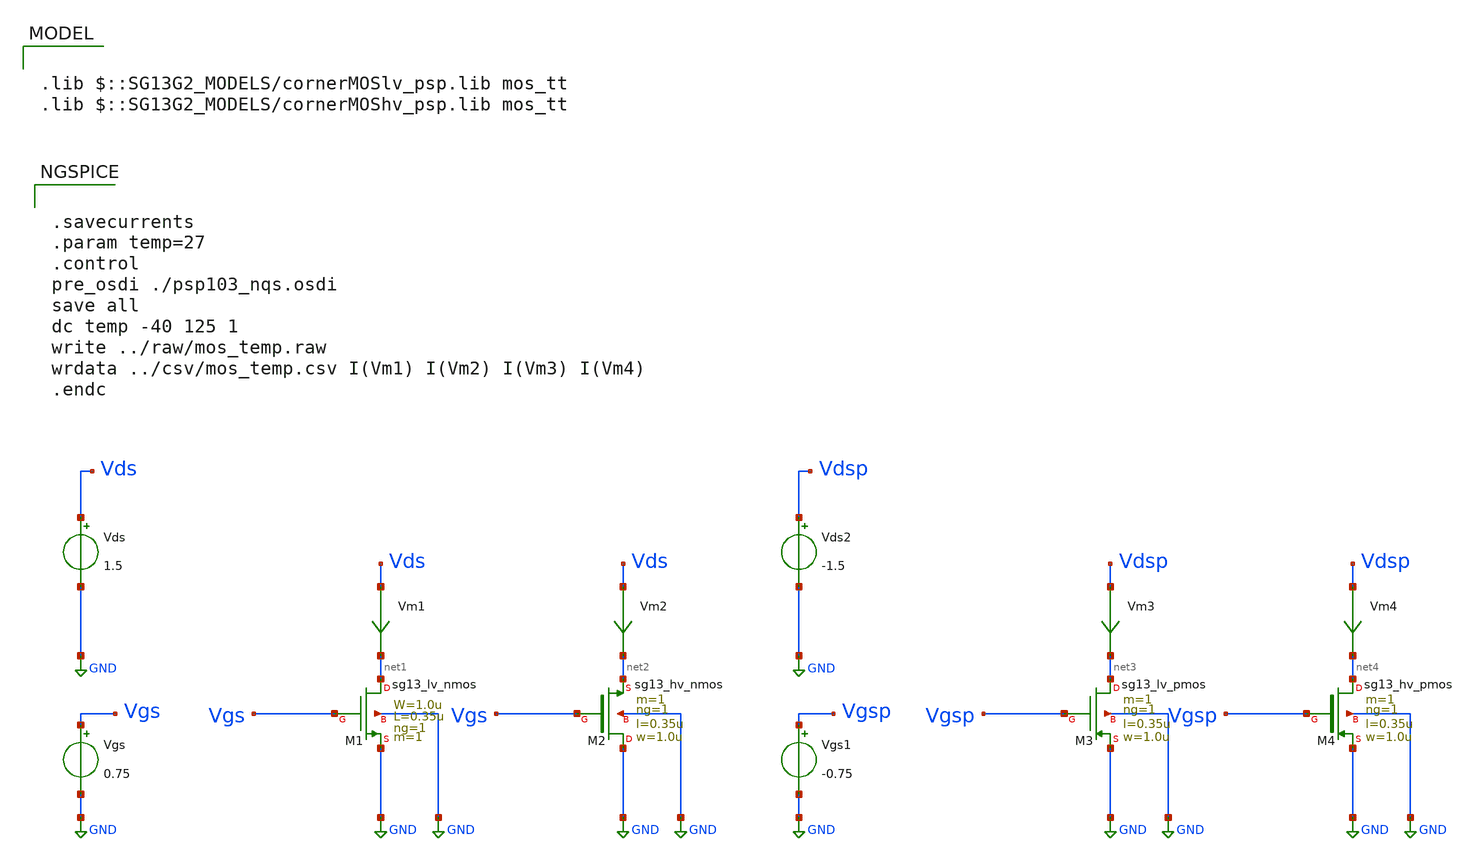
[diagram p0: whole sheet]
** sch_path: ihp-sg13g2/libs.tech/xschem/sg13g2_tests/dc_mos_temp.sch
* Copyright 2023 IHP PDK Authors
**.subckt dc_mos_temp
Vgs Vgs GND 0.75
Vds Vds GND 1.5
XM1 net1 Vgs GND GND sg13_lv_nmos W=1.0u L=0.35u ng=1 m=1
Vm1 Vds net1 0
.save i(vm1)
Vm2 Vds net2 0
.save i(vm2)
XM2 GND Vgs net2 GND sg13_hv_nmos w=1.0u l=0.35u ng=1 m=1 mm_ok=1
Vm3 Vdsp net3 0
.save i(vm3)
Vm4 Vdsp net4 0
.save i(vm4)
XM3 net3 Vgsp GND GND sg13_lv_pmos w=1.0u l=0.35u ng=1 m=1 mm_ok=1
XM4 net4 Vgsp GND GND sg13_hv_pmos w=1.0u l=0.35u ng=1 m=1 mm_ok=1
Vgs1 Vgsp GND -0.75
Vds2 Vdsp GND -1.5
**** begin user architecture code

.lib $::SG13G2_MODELS/cornerMOSlv_psp.lib mos_tt
.lib $::SG13G2_MODELS/cornerMOShv_psp.lib mos_tt



.savecurrents
.param temp=27
.control
pre_osdi ./psp103_nqs.osdi
save all
dc temp -40 125 1
write ../raw/mos_temp.raw
wrdata ../csv/mos_temp.csv I(Vm1) I(Vm2) I(Vm3) I(Vm4)
.endc


**** end user architecture code
**.ends
.GLOBAL GND
.end
